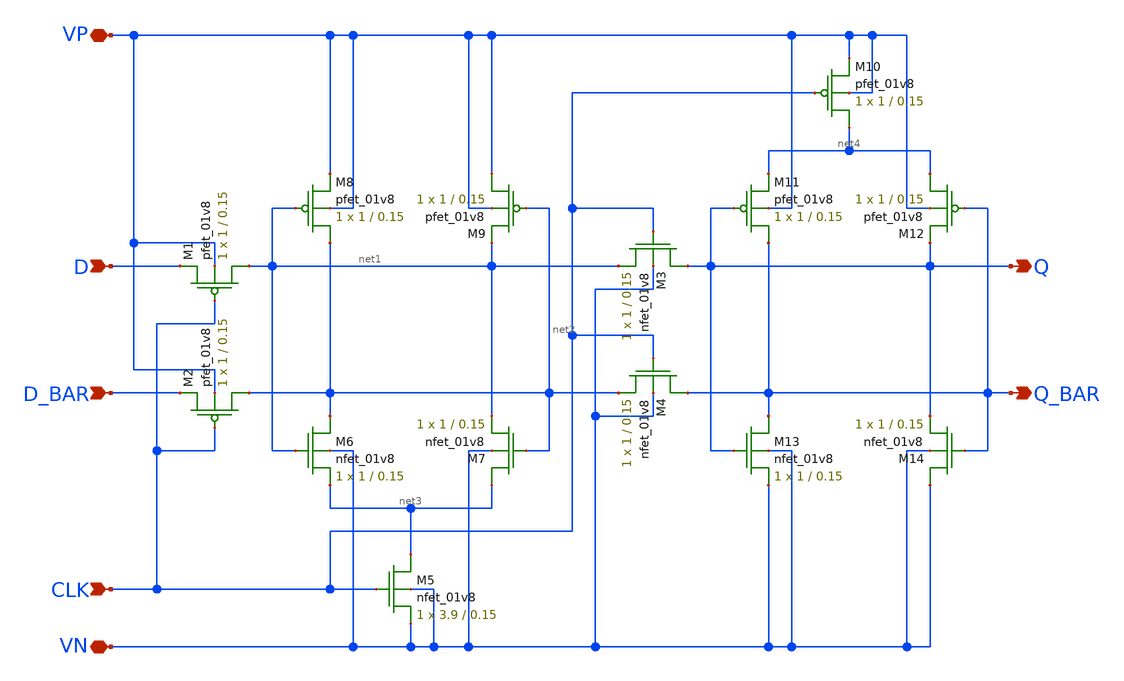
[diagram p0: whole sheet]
** sch_path: mp2/schematics/crsl_d_flip_flop.sch
**.subckt crsl_d_flip_flop D D_BAR VP VN Q Q_BAR CLK
*.ipin D
*.ipin D_BAR
*.iopin VP
*.iopin VN
*.opin Q
*.opin Q_BAR
*.ipin CLK
XM1 net1 CLK D VP sky130_fd_pr__pfet_01v8 L=0.15 W=1 nf=1 ad='int((nf+1)/2) * W/nf * 0.29' as='int((nf+2)/2) * W/nf * 0.29'
+ pd='2*int((nf+1)/2) * (W/nf + 0.29)' ps='2*int((nf+2)/2) * (W/nf + 0.29)' nrd='0.29 / W' nrs='0.29 / W'
+ sa=0 sb=0 sd=0 mult=1 m=1
XM2 net2 CLK D_BAR VP sky130_fd_pr__pfet_01v8 L=0.15 W=1 nf=1 ad='int((nf+1)/2) * W/nf * 0.29' as='int((nf+2)/2) * W/nf * 0.29'
+ pd='2*int((nf+1)/2) * (W/nf + 0.29)' ps='2*int((nf+2)/2) * (W/nf + 0.29)' nrd='0.29 / W' nrs='0.29 / W'
+ sa=0 sb=0 sd=0 mult=1 m=1
XM8 net2 net1 VP VP sky130_fd_pr__pfet_01v8 L=0.15 W=1 nf=1 ad='int((nf+1)/2) * W/nf * 0.29' as='int((nf+2)/2) * W/nf * 0.29'
+ pd='2*int((nf+1)/2) * (W/nf + 0.29)' ps='2*int((nf+2)/2) * (W/nf + 0.29)' nrd='0.29 / W' nrs='0.29 / W'
+ sa=0 sb=0 sd=0 mult=1 m=1
XM9 VP net2 net1 VP sky130_fd_pr__pfet_01v8 L=0.15 W=1 nf=1 ad='int((nf+1)/2) * W/nf * 0.29' as='int((nf+2)/2) * W/nf * 0.29'
+ pd='2*int((nf+1)/2) * (W/nf + 0.29)' ps='2*int((nf+2)/2) * (W/nf + 0.29)' nrd='0.29 / W' nrs='0.29 / W'
+ sa=0 sb=0 sd=0 mult=1 m=1
XM6 net2 net1 net3 VN sky130_fd_pr__nfet_01v8 L=0.15 W=1 nf=1 ad='int((nf+1)/2) * W/nf * 0.29' as='int((nf+2)/2) * W/nf * 0.29'
+ pd='2*int((nf+1)/2) * (W/nf + 0.29)' ps='2*int((nf+2)/2) * (W/nf + 0.29)' nrd='0.29 / W' nrs='0.29 / W'
+ sa=0 sb=0 sd=0 mult=1 m=1
XM7 net3 net2 net1 VN sky130_fd_pr__nfet_01v8 L=0.15 W=1 nf=1 ad='int((nf+1)/2) * W/nf * 0.29' as='int((nf+2)/2) * W/nf * 0.29'
+ pd='2*int((nf+1)/2) * (W/nf + 0.29)' ps='2*int((nf+2)/2) * (W/nf + 0.29)' nrd='0.29 / W' nrs='0.29 / W'
+ sa=0 sb=0 sd=0 mult=1 m=1
XM3 Q CLK net1 VN sky130_fd_pr__nfet_01v8 L=0.15 W=1 nf=1 ad='int((nf+1)/2) * W/nf * 0.29' as='int((nf+2)/2) * W/nf * 0.29'
+ pd='2*int((nf+1)/2) * (W/nf + 0.29)' ps='2*int((nf+2)/2) * (W/nf + 0.29)' nrd='0.29 / W' nrs='0.29 / W'
+ sa=0 sb=0 sd=0 mult=1 m=1
XM4 Q_BAR CLK net2 VN sky130_fd_pr__nfet_01v8 L=0.15 W=1 nf=1 ad='int((nf+1)/2) * W/nf * 0.29' as='int((nf+2)/2) * W/nf * 0.29'
+ pd='2*int((nf+1)/2) * (W/nf + 0.29)' ps='2*int((nf+2)/2) * (W/nf + 0.29)' nrd='0.29 / W' nrs='0.29 / W'
+ sa=0 sb=0 sd=0 mult=1 m=1
XM13 Q_BAR Q VN VN sky130_fd_pr__nfet_01v8 L=0.15 W=1 nf=1 ad='int((nf+1)/2) * W/nf * 0.29' as='int((nf+2)/2) * W/nf * 0.29'
+ pd='2*int((nf+1)/2) * (W/nf + 0.29)' ps='2*int((nf+2)/2) * (W/nf + 0.29)' nrd='0.29 / W' nrs='0.29 / W'
+ sa=0 sb=0 sd=0 mult=1 m=1
XM14 VN Q_BAR Q VN sky130_fd_pr__nfet_01v8 L=0.15 W=1 nf=1 ad='int((nf+1)/2) * W/nf * 0.29' as='int((nf+2)/2) * W/nf * 0.29'
+ pd='2*int((nf+1)/2) * (W/nf + 0.29)' ps='2*int((nf+2)/2) * (W/nf + 0.29)' nrd='0.29 / W' nrs='0.29 / W'
+ sa=0 sb=0 sd=0 mult=1 m=1
XM12 net4 Q_BAR Q VP sky130_fd_pr__pfet_01v8 L=0.15 W=1 nf=1 ad='int((nf+1)/2) * W/nf * 0.29' as='int((nf+2)/2) * W/nf * 0.29'
+ pd='2*int((nf+1)/2) * (W/nf + 0.29)' ps='2*int((nf+2)/2) * (W/nf + 0.29)' nrd='0.29 / W' nrs='0.29 / W'
+ sa=0 sb=0 sd=0 mult=1 m=1
XM11 Q_BAR Q net4 VP sky130_fd_pr__pfet_01v8 L=0.15 W=1 nf=1 ad='int((nf+1)/2) * W/nf * 0.29' as='int((nf+2)/2) * W/nf * 0.29'
+ pd='2*int((nf+1)/2) * (W/nf + 0.29)' ps='2*int((nf+2)/2) * (W/nf + 0.29)' nrd='0.29 / W' nrs='0.29 / W'
+ sa=0 sb=0 sd=0 mult=1 m=1
XM5 net3 CLK VN VN sky130_fd_pr__nfet_01v8 L=0.15 W=3.9 nf=1 ad='int((nf+1)/2) * W/nf * 0.29' as='int((nf+2)/2) * W/nf * 0.29'
+ pd='2*int((nf+1)/2) * (W/nf + 0.29)' ps='2*int((nf+2)/2) * (W/nf + 0.29)' nrd='0.29 / W' nrs='0.29 / W'
+ sa=0 sb=0 sd=0 mult=1 m=1
XM10 net4 CLK VP VP sky130_fd_pr__pfet_01v8 L=0.15 W=1 nf=1 ad='int((nf+1)/2) * W/nf * 0.29' as='int((nf+2)/2) * W/nf * 0.29'
+ pd='2*int((nf+1)/2) * (W/nf + 0.29)' ps='2*int((nf+2)/2) * (W/nf + 0.29)' nrd='0.29 / W' nrs='0.29 / W'
+ sa=0 sb=0 sd=0 mult=1 m=1
**.ends
.end
